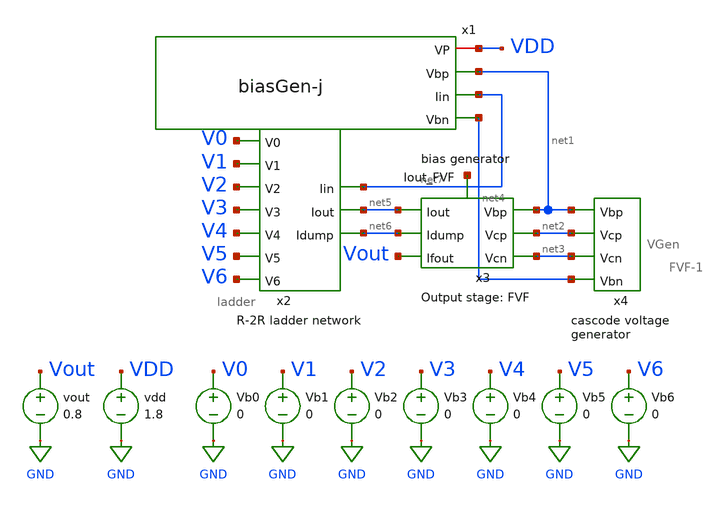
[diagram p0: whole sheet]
** sch_path: xschem/mp4_dac_simulation_andrew.sch
**.subckt mp4_dac_simulation_andrew
Vb1 V1 GND 0
Vb2 V2 GND 0
Vb3 V3 GND 0
Vb4 V4 GND 0
Vb5 V5 GND 0
Vb6 V6 GND 0
Vb0 V0 GND 0
x2 net7 net6 net5 V0 V1 V2 V3 V4 V5 V6 ladder
x3 net1 net2 net5 net3 Vout net6 net8 FVF-1
x4 net1 net3 net2 net4 VGen
vdd VDD GND 1.8
x1 VDD net1 net7 net4 biasGen-j
vout Vout GND 0.8
**** begin user architecture code

.option wnflag=1
.param MC_SWITCH=0.0
.lib ~/skywater/skywater-pdk/libraries/sky130_fd_pr_ngspice/latest/models/sky130.lib.spice tt



.control
  set wr_vecnames
  set wr_singlescale
  let code = 0
  while code < 120
    if code eq 0
      let b0 = 0
    else
      let b0 = code % 2
    end
    if floor(code / 2) eq 0
      let b1 = 0
    else
      let b1 = floor(code / 2) % 2
    end
    if floor(code / 4) eq 0
      let b2 = 0
    else
      let b2 = floor(code / 4) % 2
    end
    if floor(code / 8) eq 0
      let b3 = 0
    else
      let b3 = floor(code / 8) % 2
    end
    if floor(code / 16) eq 0
      let b4 = 0
    else
      let b4 = floor(code / 16) % 2
    end
    if floor(code / 32) eq 0
      let b5 = 0
    else
      let b5 = floor(code / 32) % 2
    end
    if floor(code / 64) eq 0
      let b6 = 0
    else
      let b6 = floor(code / 64) % 2
    end
    alter Vb0 1.8*$&b0
    alter Vb1 1.8*$&b1
    alter Vb2 1.8*$&b2
    alter Vb3 1.8*$&b3
    alter Vb4 1.8*$&b4
    alter Vb5 1.8*$&b5
    alter Vb6 1.8*$&b6
    save all
    op
    wrdata ~/Documents/DAC-VLSI/simulation_results/dac_simulation_andrew.txt v(b0) v(b1) v(b2) v(b3)
+ v(b4) v(b5) v(b6) i(Vout)
    if code eq 0
      set appendwrite
      set wr_vecnames = FALSE
    end
    let code = code + 1
  end
  quit
.endc

**** end user architecture code
**.ends

* expanding   symbol:  ./ladder.sym # of pins=10
** sym_path: xschem/ladder.sym
** sch_path: xschem/ladder.sch
.subckt ladder Iin Idump Iout V0 V1 V2 V3 V4 V5 V6
*.ipin Iin
*.ipin V0
*.ipin V1
*.ipin V2
*.ipin V3
*.ipin V4
*.ipin V5
*.ipin V6
*.opin Idump
*.opin Iout
XM1 Iin VDD net1 GND sky130_fd_pr__nfet_01v8 L=0.15 W=1 nf=1 ad='int((nf+1)/2) * W/nf * 0.29' as='int((nf+2)/2) * W/nf * 0.29'
+ pd='2*int((nf+1)/2) * (W/nf + 0.29)' ps='2*int((nf+2)/2) * (W/nf + 0.29)' nrd='0.29 / W' nrs='0.29 / W'
+ sa=0 sb=0 sd=0 mult=1 m=1
XM3 Iin VDD net3 GND sky130_fd_pr__nfet_01v8 L=0.15 W=1 nf=1 ad='int((nf+1)/2) * W/nf * 0.29' as='int((nf+2)/2) * W/nf * 0.29'
+ pd='2*int((nf+1)/2) * (W/nf + 0.29)' ps='2*int((nf+2)/2) * (W/nf + 0.29)' nrd='0.29 / W' nrs='0.29 / W'
+ sa=0 sb=0 sd=0 mult=1 m=1
XM5 net3 VDD net4 GND sky130_fd_pr__nfet_01v8 L=0.15 W=1 nf=1 ad='int((nf+1)/2) * W/nf * 0.29' as='int((nf+2)/2) * W/nf * 0.29'
+ pd='2*int((nf+1)/2) * (W/nf + 0.29)' ps='2*int((nf+2)/2) * (W/nf + 0.29)' nrd='0.29 / W' nrs='0.29 / W'
+ sa=0 sb=0 sd=0 mult=1 m=1
XM7 net3 VDD net6 GND sky130_fd_pr__nfet_01v8 L=0.15 W=1 nf=1 ad='int((nf+1)/2) * W/nf * 0.29' as='int((nf+2)/2) * W/nf * 0.29'
+ pd='2*int((nf+1)/2) * (W/nf + 0.29)' ps='2*int((nf+2)/2) * (W/nf + 0.29)' nrd='0.29 / W' nrs='0.29 / W'
+ sa=0 sb=0 sd=0 mult=1 m=1
XM6 net4 V1 net2 GND sky130_fd_pr__nfet_01v8 L=0.15 W=1 nf=1 ad='int((nf+1)/2) * W/nf * 0.29' as='int((nf+2)/2) * W/nf * 0.29'
+ pd='2*int((nf+1)/2) * (W/nf + 0.29)' ps='2*int((nf+2)/2) * (W/nf + 0.29)' nrd='0.29 / W' nrs='0.29 / W'
+ sa=0 sb=0 sd=0 mult=1 m=1
XM8 net4 net18 net5 GND sky130_fd_pr__nfet_01v8 L=0.15 W=1 nf=1 ad='int((nf+1)/2) * W/nf * 0.29' as='int((nf+2)/2) * W/nf * 0.29'
+ pd='2*int((nf+1)/2) * (W/nf + 0.29)' ps='2*int((nf+2)/2) * (W/nf + 0.29)' nrd='0.29 / W' nrs='0.29 / W'
+ sa=0 sb=0 sd=0 mult=1 m=1
XM2 net1 V0 net2 GND sky130_fd_pr__nfet_01v8 L=0.15 W=1 nf=1 ad='int((nf+1)/2) * W/nf * 0.29' as='int((nf+2)/2) * W/nf * 0.29'
+ pd='2*int((nf+1)/2) * (W/nf + 0.29)' ps='2*int((nf+2)/2) * (W/nf + 0.29)' nrd='0.29 / W' nrs='0.29 / W'
+ sa=0 sb=0 sd=0 mult=1 m=1
XM4 net1 net17 net5 GND sky130_fd_pr__nfet_01v8 L=0.15 W=1 nf=1 ad='int((nf+1)/2) * W/nf * 0.29' as='int((nf+2)/2) * W/nf * 0.29'
+ pd='2*int((nf+1)/2) * (W/nf + 0.29)' ps='2*int((nf+2)/2) * (W/nf + 0.29)' nrd='0.29 / W' nrs='0.29 / W'
+ sa=0 sb=0 sd=0 mult=1 m=1
XM9 net6 VDD net7 GND sky130_fd_pr__nfet_01v8 L=0.15 W=1 nf=1 ad='int((nf+1)/2) * W/nf * 0.29' as='int((nf+2)/2) * W/nf * 0.29'
+ pd='2*int((nf+1)/2) * (W/nf + 0.29)' ps='2*int((nf+2)/2) * (W/nf + 0.29)' nrd='0.29 / W' nrs='0.29 / W'
+ sa=0 sb=0 sd=0 mult=1 m=1
XM11 net6 VDD net8 GND sky130_fd_pr__nfet_01v8 L=0.15 W=1 nf=1 ad='int((nf+1)/2) * W/nf * 0.29' as='int((nf+2)/2) * W/nf * 0.29'
+ pd='2*int((nf+1)/2) * (W/nf + 0.29)' ps='2*int((nf+2)/2) * (W/nf + 0.29)' nrd='0.29 / W' nrs='0.29 / W'
+ sa=0 sb=0 sd=0 mult=1 m=1
XM10 net7 V2 net2 GND sky130_fd_pr__nfet_01v8 L=0.15 W=1 nf=1 ad='int((nf+1)/2) * W/nf * 0.29' as='int((nf+2)/2) * W/nf * 0.29'
+ pd='2*int((nf+1)/2) * (W/nf + 0.29)' ps='2*int((nf+2)/2) * (W/nf + 0.29)' nrd='0.29 / W' nrs='0.29 / W'
+ sa=0 sb=0 sd=0 mult=1 m=1
XM12 net7 net19 net5 GND sky130_fd_pr__nfet_01v8 L=0.15 W=1 nf=1 ad='int((nf+1)/2) * W/nf * 0.29' as='int((nf+2)/2) * W/nf * 0.29'
+ pd='2*int((nf+1)/2) * (W/nf + 0.29)' ps='2*int((nf+2)/2) * (W/nf + 0.29)' nrd='0.29 / W' nrs='0.29 / W'
+ sa=0 sb=0 sd=0 mult=1 m=1
XM13 net8 VDD net9 GND sky130_fd_pr__nfet_01v8 L=0.15 W=1 nf=1 ad='int((nf+1)/2) * W/nf * 0.29' as='int((nf+2)/2) * W/nf * 0.29'
+ pd='2*int((nf+1)/2) * (W/nf + 0.29)' ps='2*int((nf+2)/2) * (W/nf + 0.29)' nrd='0.29 / W' nrs='0.29 / W'
+ sa=0 sb=0 sd=0 mult=1 m=1
XM15 net8 VDD net10 GND sky130_fd_pr__nfet_01v8 L=0.15 W=1 nf=1 ad='int((nf+1)/2) * W/nf * 0.29' as='int((nf+2)/2) * W/nf * 0.29'
+ pd='2*int((nf+1)/2) * (W/nf + 0.29)' ps='2*int((nf+2)/2) * (W/nf + 0.29)' nrd='0.29 / W' nrs='0.29 / W'
+ sa=0 sb=0 sd=0 mult=1 m=1
XM14 net9 V3 net2 GND sky130_fd_pr__nfet_01v8 L=0.15 W=1 nf=1 ad='int((nf+1)/2) * W/nf * 0.29' as='int((nf+2)/2) * W/nf * 0.29'
+ pd='2*int((nf+1)/2) * (W/nf + 0.29)' ps='2*int((nf+2)/2) * (W/nf + 0.29)' nrd='0.29 / W' nrs='0.29 / W'
+ sa=0 sb=0 sd=0 mult=1 m=1
XM16 net9 net20 net5 GND sky130_fd_pr__nfet_01v8 L=0.15 W=1 nf=1 ad='int((nf+1)/2) * W/nf * 0.29' as='int((nf+2)/2) * W/nf * 0.29'
+ pd='2*int((nf+1)/2) * (W/nf + 0.29)' ps='2*int((nf+2)/2) * (W/nf + 0.29)' nrd='0.29 / W' nrs='0.29 / W'
+ sa=0 sb=0 sd=0 mult=1 m=1
XM17 net10 VDD net11 GND sky130_fd_pr__nfet_01v8 L=0.15 W=1 nf=1 ad='int((nf+1)/2) * W/nf * 0.29' as='int((nf+2)/2) * W/nf * 0.29'
+ pd='2*int((nf+1)/2) * (W/nf + 0.29)' ps='2*int((nf+2)/2) * (W/nf + 0.29)' nrd='0.29 / W' nrs='0.29 / W'
+ sa=0 sb=0 sd=0 mult=1 m=1
XM19 net10 VDD net12 GND sky130_fd_pr__nfet_01v8 L=0.15 W=1 nf=1 ad='int((nf+1)/2) * W/nf * 0.29' as='int((nf+2)/2) * W/nf * 0.29'
+ pd='2*int((nf+1)/2) * (W/nf + 0.29)' ps='2*int((nf+2)/2) * (W/nf + 0.29)' nrd='0.29 / W' nrs='0.29 / W'
+ sa=0 sb=0 sd=0 mult=1 m=1
XM18 net11 V4 net2 GND sky130_fd_pr__nfet_01v8 L=0.15 W=1 nf=1 ad='int((nf+1)/2) * W/nf * 0.29' as='int((nf+2)/2) * W/nf * 0.29'
+ pd='2*int((nf+1)/2) * (W/nf + 0.29)' ps='2*int((nf+2)/2) * (W/nf + 0.29)' nrd='0.29 / W' nrs='0.29 / W'
+ sa=0 sb=0 sd=0 mult=1 m=1
XM20 net11 net21 net5 GND sky130_fd_pr__nfet_01v8 L=0.15 W=1 nf=1 ad='int((nf+1)/2) * W/nf * 0.29' as='int((nf+2)/2) * W/nf * 0.29'
+ pd='2*int((nf+1)/2) * (W/nf + 0.29)' ps='2*int((nf+2)/2) * (W/nf + 0.29)' nrd='0.29 / W' nrs='0.29 / W'
+ sa=0 sb=0 sd=0 mult=1 m=1
XM21 net12 VDD net13 GND sky130_fd_pr__nfet_01v8 L=0.15 W=1 nf=1 ad='int((nf+1)/2) * W/nf * 0.29' as='int((nf+2)/2) * W/nf * 0.29'
+ pd='2*int((nf+1)/2) * (W/nf + 0.29)' ps='2*int((nf+2)/2) * (W/nf + 0.29)' nrd='0.29 / W' nrs='0.29 / W'
+ sa=0 sb=0 sd=0 mult=1 m=1
XM23 net12 VDD net14 GND sky130_fd_pr__nfet_01v8 L=0.15 W=1 nf=1 ad='int((nf+1)/2) * W/nf * 0.29' as='int((nf+2)/2) * W/nf * 0.29'
+ pd='2*int((nf+1)/2) * (W/nf + 0.29)' ps='2*int((nf+2)/2) * (W/nf + 0.29)' nrd='0.29 / W' nrs='0.29 / W'
+ sa=0 sb=0 sd=0 mult=1 m=1
XM22 net13 V5 net2 GND sky130_fd_pr__nfet_01v8 L=0.15 W=1 nf=1 ad='int((nf+1)/2) * W/nf * 0.29' as='int((nf+2)/2) * W/nf * 0.29'
+ pd='2*int((nf+1)/2) * (W/nf + 0.29)' ps='2*int((nf+2)/2) * (W/nf + 0.29)' nrd='0.29 / W' nrs='0.29 / W'
+ sa=0 sb=0 sd=0 mult=1 m=1
XM24 net13 net22 net5 GND sky130_fd_pr__nfet_01v8 L=0.15 W=1 nf=1 ad='int((nf+1)/2) * W/nf * 0.29' as='int((nf+2)/2) * W/nf * 0.29'
+ pd='2*int((nf+1)/2) * (W/nf + 0.29)' ps='2*int((nf+2)/2) * (W/nf + 0.29)' nrd='0.29 / W' nrs='0.29 / W'
+ sa=0 sb=0 sd=0 mult=1 m=1
XM25 net14 VDD net15 GND sky130_fd_pr__nfet_01v8 L=0.15 W=1 nf=1 ad='int((nf+1)/2) * W/nf * 0.29' as='int((nf+2)/2) * W/nf * 0.29'
+ pd='2*int((nf+1)/2) * (W/nf + 0.29)' ps='2*int((nf+2)/2) * (W/nf + 0.29)' nrd='0.29 / W' nrs='0.29 / W'
+ sa=0 sb=0 sd=0 mult=1 m=1
XM27 net14 VDD net16 GND sky130_fd_pr__nfet_01v8 L=0.15 W=1 nf=1 ad='int((nf+1)/2) * W/nf * 0.29' as='int((nf+2)/2) * W/nf * 0.29'
+ pd='2*int((nf+1)/2) * (W/nf + 0.29)' ps='2*int((nf+2)/2) * (W/nf + 0.29)' nrd='0.29 / W' nrs='0.29 / W'
+ sa=0 sb=0 sd=0 mult=1 m=1
XM26 net15 V6 net2 GND sky130_fd_pr__nfet_01v8 L=0.15 W=1 nf=1 ad='int((nf+1)/2) * W/nf * 0.29' as='int((nf+2)/2) * W/nf * 0.29'
+ pd='2*int((nf+1)/2) * (W/nf + 0.29)' ps='2*int((nf+2)/2) * (W/nf + 0.29)' nrd='0.29 / W' nrs='0.29 / W'
+ sa=0 sb=0 sd=0 mult=1 m=1
XM28 net15 net23 net5 GND sky130_fd_pr__nfet_01v8 L=0.15 W=1 nf=1 ad='int((nf+1)/2) * W/nf * 0.29' as='int((nf+2)/2) * W/nf * 0.29'
+ pd='2*int((nf+1)/2) * (W/nf + 0.29)' ps='2*int((nf+2)/2) * (W/nf + 0.29)' nrd='0.29 / W' nrs='0.29 / W'
+ sa=0 sb=0 sd=0 mult=1 m=1
XM29 net16 VDD net5 GND sky130_fd_pr__nfet_01v8 L=0.15 W=1 nf=1 ad='int((nf+1)/2) * W/nf * 0.29' as='int((nf+2)/2) * W/nf * 0.29'
+ pd='2*int((nf+1)/2) * (W/nf + 0.29)' ps='2*int((nf+2)/2) * (W/nf + 0.29)' nrd='0.29 / W' nrs='0.29 / W'
+ sa=0 sb=0 sd=0 mult=1 m=1
XM30 GND net5 net5 GND sky130_fd_pr__nfet_01v8 L=0.15 W=1 nf=1 ad='int((nf+1)/2) * W/nf * 0.29' as='int((nf+2)/2) * W/nf * 0.29'
+ pd='2*int((nf+1)/2) * (W/nf + 0.29)' ps='2*int((nf+2)/2) * (W/nf + 0.29)' nrd='0.29 / W' nrs='0.29 / W'
+ sa=0 sb=0 sd=0 mult=1 m=1
XM31 GND net2 net2 GND sky130_fd_pr__nfet_01v8 L=0.15 W=1 nf=1 ad='int((nf+1)/2) * W/nf * 0.29' as='int((nf+2)/2) * W/nf * 0.29'
+ pd='2*int((nf+1)/2) * (W/nf + 0.29)' ps='2*int((nf+2)/2) * (W/nf + 0.29)' nrd='0.29 / W' nrs='0.29 / W'
+ sa=0 sb=0 sd=0 mult=1 m=1
XM32 Idump net5 GND GND sky130_fd_pr__nfet_01v8 L=0.15 W=1 nf=1 ad='int((nf+1)/2) * W/nf * 0.29' as='int((nf+2)/2) * W/nf * 0.29'
+ pd='2*int((nf+1)/2) * (W/nf + 0.29)' ps='2*int((nf+2)/2) * (W/nf + 0.29)' nrd='0.29 / W' nrs='0.29 / W'
+ sa=0 sb=0 sd=0 mult=1 m=1
XM33 Iout net2 GND GND sky130_fd_pr__nfet_01v8 L=0.15 W=1 nf=1 ad='int((nf+1)/2) * W/nf * 0.29' as='int((nf+2)/2) * W/nf * 0.29'
+ pd='2*int((nf+1)/2) * (W/nf + 0.29)' ps='2*int((nf+2)/2) * (W/nf + 0.29)' nrd='0.29 / W' nrs='0.29 / W'
+ sa=0 sb=0 sd=0 mult=1 m=1
x1 net17 V0 inverter
x2 net18 V1 inverter
x3 net19 V2 inverter
x4 net20 V3 inverter
x5 net21 V4 inverter
x6 net22 V5 inverter
x7 net23 V6 inverter
.ends


* expanding   symbol:  ./FVF-1.sym # of pins=7
** sym_path: xschem/old_files/FVF-1.sym
** sch_path: xschem/old_files/FVF-1.sch
.subckt FVF-1 Vbp Vcp Iout Vcn Ifout Idump Iout_FVF
*.ipin Vcn
*.ipin Iout
*.ipin Idump
*.ipin Vcp
*.ipin Vbp
*.opin Ifout
*.opin Iout_FVF
XM1 net1 Vcn Idump GND sky130_fd_pr__nfet_01v8 L=8 W=24 nf=1 ad='int((nf+1)/2) * W/nf * 0.29' as='int((nf+2)/2) * W/nf * 0.29'
+ pd='2*int((nf+1)/2) * (W/nf + 0.29)' ps='2*int((nf+2)/2) * (W/nf + 0.29)' nrd='0.29 / W' nrs='0.29 / W'
+ sa=0 sb=0 sd=0 mult=1 m=1
XM2 GND net1 Idump GND sky130_fd_pr__nfet_01v8 L=8 W=24 nf=1 ad='int((nf+1)/2) * W/nf * 0.29' as='int((nf+2)/2) * W/nf * 0.29'
+ pd='2*int((nf+1)/2) * (W/nf + 0.29)' ps='2*int((nf+2)/2) * (W/nf + 0.29)' nrd='0.29 / W' nrs='0.29 / W'
+ sa=0 sb=0 sd=0 mult=1 m=1
XM3 Iout_FVF Vcn Iout GND sky130_fd_pr__nfet_01v8 L=8 W=24 nf=1 ad='int((nf+1)/2) * W/nf * 0.29' as='int((nf+2)/2) * W/nf * 0.29'
+ pd='2*int((nf+1)/2) * (W/nf + 0.29)' ps='2*int((nf+2)/2) * (W/nf + 0.29)' nrd='0.29 / W' nrs='0.29 / W'
+ sa=0 sb=0 sd=0 mult=1 m=1
XM4 GND Iout_FVF Iout GND sky130_fd_pr__nfet_01v8 L=8 W=24 nf=1 ad='int((nf+1)/2) * W/nf * 0.29' as='int((nf+2)/2) * W/nf * 0.29'
+ pd='2*int((nf+1)/2) * (W/nf + 0.29)' ps='2*int((nf+2)/2) * (W/nf + 0.29)' nrd='0.29 / W' nrs='0.29 / W'
+ sa=0 sb=0 sd=0 mult=1 m=1
XM5 Ifout Vcn net2 GND sky130_fd_pr__nfet_01v8 L=8 W=24 nf=1 ad='int((nf+1)/2) * W/nf * 0.29' as='int((nf+2)/2) * W/nf * 0.29'
+ pd='2*int((nf+1)/2) * (W/nf + 0.29)' ps='2*int((nf+2)/2) * (W/nf + 0.29)' nrd='0.29 / W' nrs='0.29 / W'
+ sa=0 sb=0 sd=0 mult=1 m=1
XM6 net2 Iout_FVF GND GND sky130_fd_pr__nfet_01v8 L=8 W=24 nf=1 ad='int((nf+1)/2) * W/nf * 0.29' as='int((nf+2)/2) * W/nf * 0.29'
+ pd='2*int((nf+1)/2) * (W/nf + 0.29)' ps='2*int((nf+2)/2) * (W/nf + 0.29)' nrd='0.29 / W' nrs='0.29 / W'
+ sa=0 sb=0 sd=0 mult=1 m=1
XM7 net1 Vcp net3 VDD sky130_fd_pr__pfet_01v8 L=8 W=24 nf=1 ad='int((nf+1)/2) * W/nf * 0.29' as='int((nf+2)/2) * W/nf * 0.29'
+ pd='2*int((nf+1)/2) * (W/nf + 0.29)' ps='2*int((nf+2)/2) * (W/nf + 0.29)' nrd='0.29 / W' nrs='0.29 / W'
+ sa=0 sb=0 sd=0 mult=1 m=1
XM8 Iout_FVF Vcp net4 VDD sky130_fd_pr__pfet_01v8 L=8 W=24 nf=1 ad='int((nf+1)/2) * W/nf * 0.29' as='int((nf+2)/2) * W/nf * 0.29'
+ pd='2*int((nf+1)/2) * (W/nf + 0.29)' ps='2*int((nf+2)/2) * (W/nf + 0.29)' nrd='0.29 / W' nrs='0.29 / W'
+ sa=0 sb=0 sd=0 mult=1 m=1
XM9 Ifout Vcp net5 VDD sky130_fd_pr__pfet_01v8 L=8 W=24 nf=1 ad='int((nf+1)/2) * W/nf * 0.29' as='int((nf+2)/2) * W/nf * 0.29'
+ pd='2*int((nf+1)/2) * (W/nf + 0.29)' ps='2*int((nf+2)/2) * (W/nf + 0.29)' nrd='0.29 / W' nrs='0.29 / W'
+ sa=0 sb=0 sd=0 mult=1 m=1
XM15 net3 Vbp VDD VDD sky130_fd_pr__pfet_01v8 L=8 W=24 nf=1 ad='int((nf+1)/2) * W/nf * 0.29' as='int((nf+2)/2) * W/nf * 0.29'
+ pd='2*int((nf+1)/2) * (W/nf + 0.29)' ps='2*int((nf+2)/2) * (W/nf + 0.29)' nrd='0.29 / W' nrs='0.29 / W'
+ sa=0 sb=0 sd=0 mult=1 m=1
XM16 net4 Vbp VDD VDD sky130_fd_pr__pfet_01v8 L=8 W=24 nf=1 ad='int((nf+1)/2) * W/nf * 0.29' as='int((nf+2)/2) * W/nf * 0.29'
+ pd='2*int((nf+1)/2) * (W/nf + 0.29)' ps='2*int((nf+2)/2) * (W/nf + 0.29)' nrd='0.29 / W' nrs='0.29 / W'
+ sa=0 sb=0 sd=0 mult=1 m=1
XM17 net5 Vbp VDD VDD sky130_fd_pr__pfet_01v8 L=8 W=24 nf=1 ad='int((nf+1)/2) * W/nf * 0.29' as='int((nf+2)/2) * W/nf * 0.29'
+ pd='2*int((nf+1)/2) * (W/nf + 0.29)' ps='2*int((nf+2)/2) * (W/nf + 0.29)' nrd='0.29 / W' nrs='0.29 / W'
+ sa=0 sb=0 sd=0 mult=1 m=1
.ends


* expanding   symbol:  ./VGen.sym # of pins=4
** sym_path: xschem/VGen.sym
** sch_path: xschem/VGen.sch
.subckt VGen Vbp Vcn Vcp Vbn
*.opin Vcp
*.ipin Vbp
*.ipin Vbn
*.opin Vcn
XM5 net4 net4 net1 GND sky130_fd_pr__nfet_01v8 L=8 W=96 nf=1 ad='int((nf+1)/2) * W/nf * 0.29' as='int((nf+2)/2) * W/nf * 0.29'
+ pd='2*int((nf+1)/2) * (W/nf + 0.29)' ps='2*int((nf+2)/2) * (W/nf + 0.29)' nrd='0.29 / W' nrs='0.29 / W'
+ sa=0 sb=0 sd=0 mult=1 m=1
XM6 net1 net4 GND GND sky130_fd_pr__nfet_01v8 L=8 W=24 nf=1 ad='int((nf+1)/2) * W/nf * 0.29' as='int((nf+2)/2) * W/nf * 0.29'
+ pd='2*int((nf+1)/2) * (W/nf + 0.29)' ps='2*int((nf+2)/2) * (W/nf + 0.29)' nrd='0.29 / W' nrs='0.29 / W'
+ sa=0 sb=0 sd=0 mult=1 m=1
XM4 net1 Vcn Vcn GND sky130_fd_pr__nfet_01v8 L=8 W=24 nf=1 ad='int((nf+1)/2) * W/nf * 0.29' as='int((nf+2)/2) * W/nf * 0.29'
+ pd='2*int((nf+1)/2) * (W/nf + 0.29)' ps='2*int((nf+2)/2) * (W/nf + 0.29)' nrd='0.29 / W' nrs='0.29 / W'
+ sa=0 sb=0 sd=0 mult=1 m=1
XM1 VDD Vbp net4 VDD sky130_fd_pr__pfet_01v8 L=32 W=24 nf=1 ad='int((nf+1)/2) * W/nf * 0.29' as='int((nf+2)/2) * W/nf * 0.29'
+ pd='2*int((nf+1)/2) * (W/nf + 0.29)' ps='2*int((nf+2)/2) * (W/nf + 0.29)' nrd='0.29 / W' nrs='0.29 / W'
+ sa=0 sb=0 sd=0 mult=1 m=1
XM2 VDD Vbp Vcn VDD sky130_fd_pr__pfet_01v8 L=8 W=24 nf=1 ad='int((nf+1)/2) * W/nf * 0.29' as='int((nf+2)/2) * W/nf * 0.29'
+ pd='2*int((nf+1)/2) * (W/nf + 0.29)' ps='2*int((nf+2)/2) * (W/nf + 0.29)' nrd='0.29 / W' nrs='0.29 / W'
+ sa=0 sb=0 sd=0 mult=1 m=1
XM9 net3 net3 net2 VDD sky130_fd_pr__pfet_01v8 L=8 W=96 nf=1 ad='int((nf+1)/2) * W/nf * 0.29' as='int((nf+2)/2) * W/nf * 0.29'
+ pd='2*int((nf+1)/2) * (W/nf + 0.29)' ps='2*int((nf+2)/2) * (W/nf + 0.29)' nrd='0.29 / W' nrs='0.29 / W'
+ sa=0 sb=0 sd=0 mult=1 m=1
XM11 GND Vbn Vcp GND sky130_fd_pr__nfet_01v8 L=8 W=24 nf=1 ad='int((nf+1)/2) * W/nf * 0.29' as='int((nf+2)/2) * W/nf * 0.29'
+ pd='2*int((nf+1)/2) * (W/nf + 0.29)' ps='2*int((nf+2)/2) * (W/nf + 0.29)' nrd='0.29 / W' nrs='0.29 / W'
+ sa=0 sb=0 sd=0 mult=1 m=1
XM8 net2 Vcp Vcp VDD sky130_fd_pr__pfet_01v8 L=8 W=24 nf=1 ad='int((nf+1)/2) * W/nf * 0.29' as='int((nf+2)/2) * W/nf * 0.29'
+ pd='2*int((nf+1)/2) * (W/nf + 0.29)' ps='2*int((nf+2)/2) * (W/nf + 0.29)' nrd='0.29 / W' nrs='0.29 / W'
+ sa=0 sb=0 sd=0 mult=1 m=1
XM12 GND Vbn net3 GND sky130_fd_pr__nfet_01v8 L=32 W=24 nf=1 ad='int((nf+1)/2) * W/nf * 0.29' as='int((nf+2)/2) * W/nf * 0.29'
+ pd='2*int((nf+1)/2) * (W/nf + 0.29)' ps='2*int((nf+2)/2) * (W/nf + 0.29)' nrd='0.29 / W' nrs='0.29 / W'
+ sa=0 sb=0 sd=0 mult=1 m=1
XM7 net2 net3 VDD VDD sky130_fd_pr__pfet_01v8 L=8 W=24 nf=1 ad='int((nf+1)/2) * W/nf * 0.29' as='int((nf+2)/2) * W/nf * 0.29'
+ pd='2*int((nf+1)/2) * (W/nf + 0.29)' ps='2*int((nf+2)/2) * (W/nf + 0.29)' nrd='0.29 / W' nrs='0.29 / W'
+ sa=0 sb=0 sd=0 mult=1 m=1
.ends


* expanding   symbol:  /home/madvlsi/Documents/DAC-VLSI/xschem/biasGen-j.sym # of pins=4
** sym_path: xschem/biasGen-j.sym
** sch_path: xschem/biasGen-j.sch
.subckt biasGen-j VP Vbp Iin Vbn
*.opin Iin
*.opin Vbp
*.opin Vbn
*.iopin VP
XM1 Vbn Vbn GND GND sky130_fd_pr__nfet_01v8 L=4 W=24 nf=1 ad='int((nf+1)/2) * W/nf * 0.29' as='int((nf+2)/2) * W/nf * 0.29'
+ pd='2*int((nf+1)/2) * (W/nf + 0.29)' ps='2*int((nf+2)/2) * (W/nf + 0.29)' nrd='0.29 / W' nrs='0.29 / W'
+ sa=0 sb=0 sd=0 mult=1 m=1
XM2 GND Vbn Vbp GND sky130_fd_pr__nfet_01v8 L=4 W=24 nf=1 ad='int((nf+1)/2) * W/nf * 0.29' as='int((nf+2)/2) * W/nf * 0.29'
+ pd='2*int((nf+1)/2) * (W/nf + 0.29)' ps='2*int((nf+2)/2) * (W/nf + 0.29)' nrd='0.29 / W' nrs='0.29 / W'
+ sa=0 sb=0 sd=0 mult=1 m=1
XM3 net1 net2 GND GND sky130_fd_pr__nfet_01v8 L=4 W=24 nf=1 ad='int((nf+1)/2) * W/nf * 0.29' as='int((nf+2)/2) * W/nf * 0.29'
+ pd='2*int((nf+1)/2) * (W/nf + 0.29)' ps='2*int((nf+2)/2) * (W/nf + 0.29)' nrd='0.29 / W' nrs='0.29 / W'
+ sa=0 sb=0 sd=0 mult=1 m=1
XM4 net3 net2 net2 GND sky130_fd_pr__nfet_01v8 L=4 W=24 nf=1 ad='int((nf+1)/2) * W/nf * 0.29' as='int((nf+2)/2) * W/nf * 0.29'
+ pd='2*int((nf+1)/2) * (W/nf + 0.29)' ps='2*int((nf+2)/2) * (W/nf + 0.29)' nrd='0.29 / W' nrs='0.29 / W'
+ sa=0 sb=0 sd=0 mult=8 m=8
XM5 Vbp net1 VP VDD sky130_fd_pr__pfet_01v8 L=4 W=24 nf=1 ad='int((nf+1)/2) * W/nf * 0.29' as='int((nf+2)/2) * W/nf * 0.29'
+ pd='2*int((nf+1)/2) * (W/nf + 0.29)' ps='2*int((nf+2)/2) * (W/nf + 0.29)' nrd='0.29 / W' nrs='0.29 / W'
+ sa=0 sb=0 sd=0 mult=1 m=1
XM6 VP net1 net1 VDD sky130_fd_pr__pfet_01v8 L=4 W=24 nf=1 ad='int((nf+1)/2) * W/nf * 0.29' as='int((nf+2)/2) * W/nf * 0.29'
+ pd='2*int((nf+1)/2) * (W/nf + 0.29)' ps='2*int((nf+2)/2) * (W/nf + 0.29)' nrd='0.29 / W' nrs='0.29 / W'
+ sa=0 sb=0 sd=0 mult=1 m=1
XM7 VP Vbp net2 VDD sky130_fd_pr__pfet_01v8 L=4 W=24 nf=1 ad='int((nf+1)/2) * W/nf * 0.29' as='int((nf+2)/2) * W/nf * 0.29'
+ pd='2*int((nf+1)/2) * (W/nf + 0.29)' ps='2*int((nf+2)/2) * (W/nf + 0.29)' nrd='0.29 / W' nrs='0.29 / W'
+ sa=0 sb=0 sd=0 mult=1 m=1
XM8 Vbn Vbp VP VDD sky130_fd_pr__pfet_01v8 L=4 W=24 nf=1 ad='int((nf+1)/2) * W/nf * 0.29' as='int((nf+2)/2) * W/nf * 0.29'
+ pd='2*int((nf+1)/2) * (W/nf + 0.29)' ps='2*int((nf+2)/2) * (W/nf + 0.29)' nrd='0.29 / W' nrs='0.29 / W'
+ sa=0 sb=0 sd=0 mult=1 m=1
R1 net3 GND 50k m=1
XM9 Iin Vbp VP VDD sky130_fd_pr__pfet_01v8 L=4 W=24 nf=1 ad='int((nf+1)/2) * W/nf * 0.29' as='int((nf+2)/2) * W/nf * 0.29'
+ pd='2*int((nf+1)/2) * (W/nf + 0.29)' ps='2*int((nf+2)/2) * (W/nf + 0.29)' nrd='0.29 / W' nrs='0.29 / W'
+ sa=0 sb=0 sd=0 mult=1 m=1
.ends


* expanding   symbol:  ./inverter.sym # of pins=2
** sym_path: xschem/inverter.sym
** sch_path: xschem/inverter.sch
.subckt inverter Y A
*.ipin A
*.opin Y
XM1 Y A VDD VDD sky130_fd_pr__pfet_01v8 L=0.15 W=1 nf=1 ad='int((nf+1)/2) * W/nf * 0.29' as='int((nf+2)/2) * W/nf * 0.29'
+ pd='2*int((nf+1)/2) * (W/nf + 0.29)' ps='2*int((nf+2)/2) * (W/nf + 0.29)' nrd='0.29 / W' nrs='0.29 / W'
+ sa=0 sb=0 sd=0 mult=1 m=1
XM2 Y A GND GND sky130_fd_pr__nfet_01v8 L=0.15 W=1 nf=1 ad='int((nf+1)/2) * W/nf * 0.29' as='int((nf+2)/2) * W/nf * 0.29'
+ pd='2*int((nf+1)/2) * (W/nf + 0.29)' ps='2*int((nf+2)/2) * (W/nf + 0.29)' nrd='0.29 / W' nrs='0.29 / W'
+ sa=0 sb=0 sd=0 mult=1 m=1
.ends

.GLOBAL GND
.GLOBAL VDD
.end
